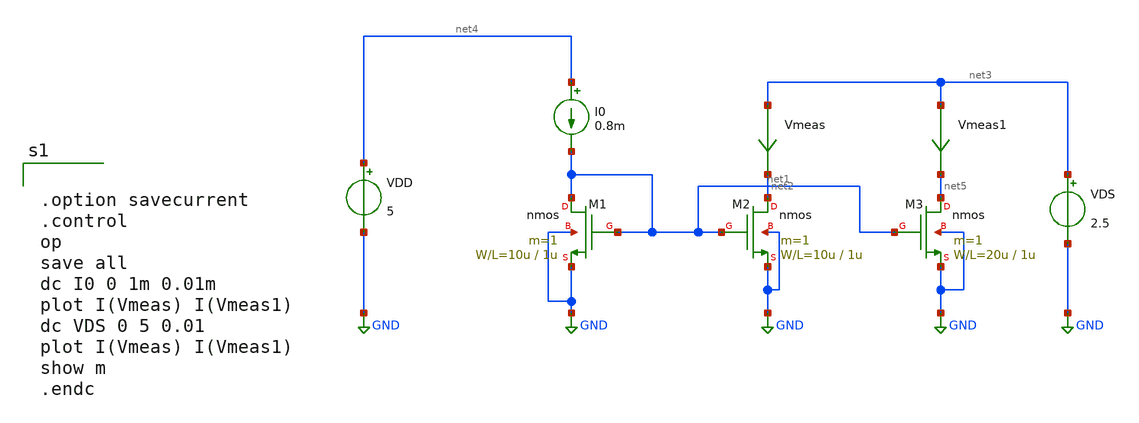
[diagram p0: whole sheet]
** sch_path: member_project/GroupWork/Team_masahiro/current_mirror_2w.sch
**.subckt current_mirror_2w
M1 net1 net1 GND GND nmos L=1u W=10u m=1
I0 net4 net1 0.8m
M2 net2 net1 GND GND nmos L=1u W=10u m=1
VDS net3 GND 2.5
VDD net4 GND 5
M3 net5 net1 GND GND nmos L=1u W=20u m=1
Vmeas net3 net2 0
.save i(vmeas)
Vmeas1 net3 net5 0
.save i(vmeas1)
**** begin user architecture code
 .include $::LIB/mos.lib
.include $::LIB/passive.lib
.include $::LIB/diode.lib


.option savecurrent
.control
op
save all
dc I0 0 1m 0.01m
plot I(Vmeas) I(Vmeas1)
dc VDS 0 5 0.01
plot I(Vmeas) I(Vmeas1)
show m
.endc


**** end user architecture code
**.ends
.GLOBAL GND
.end
